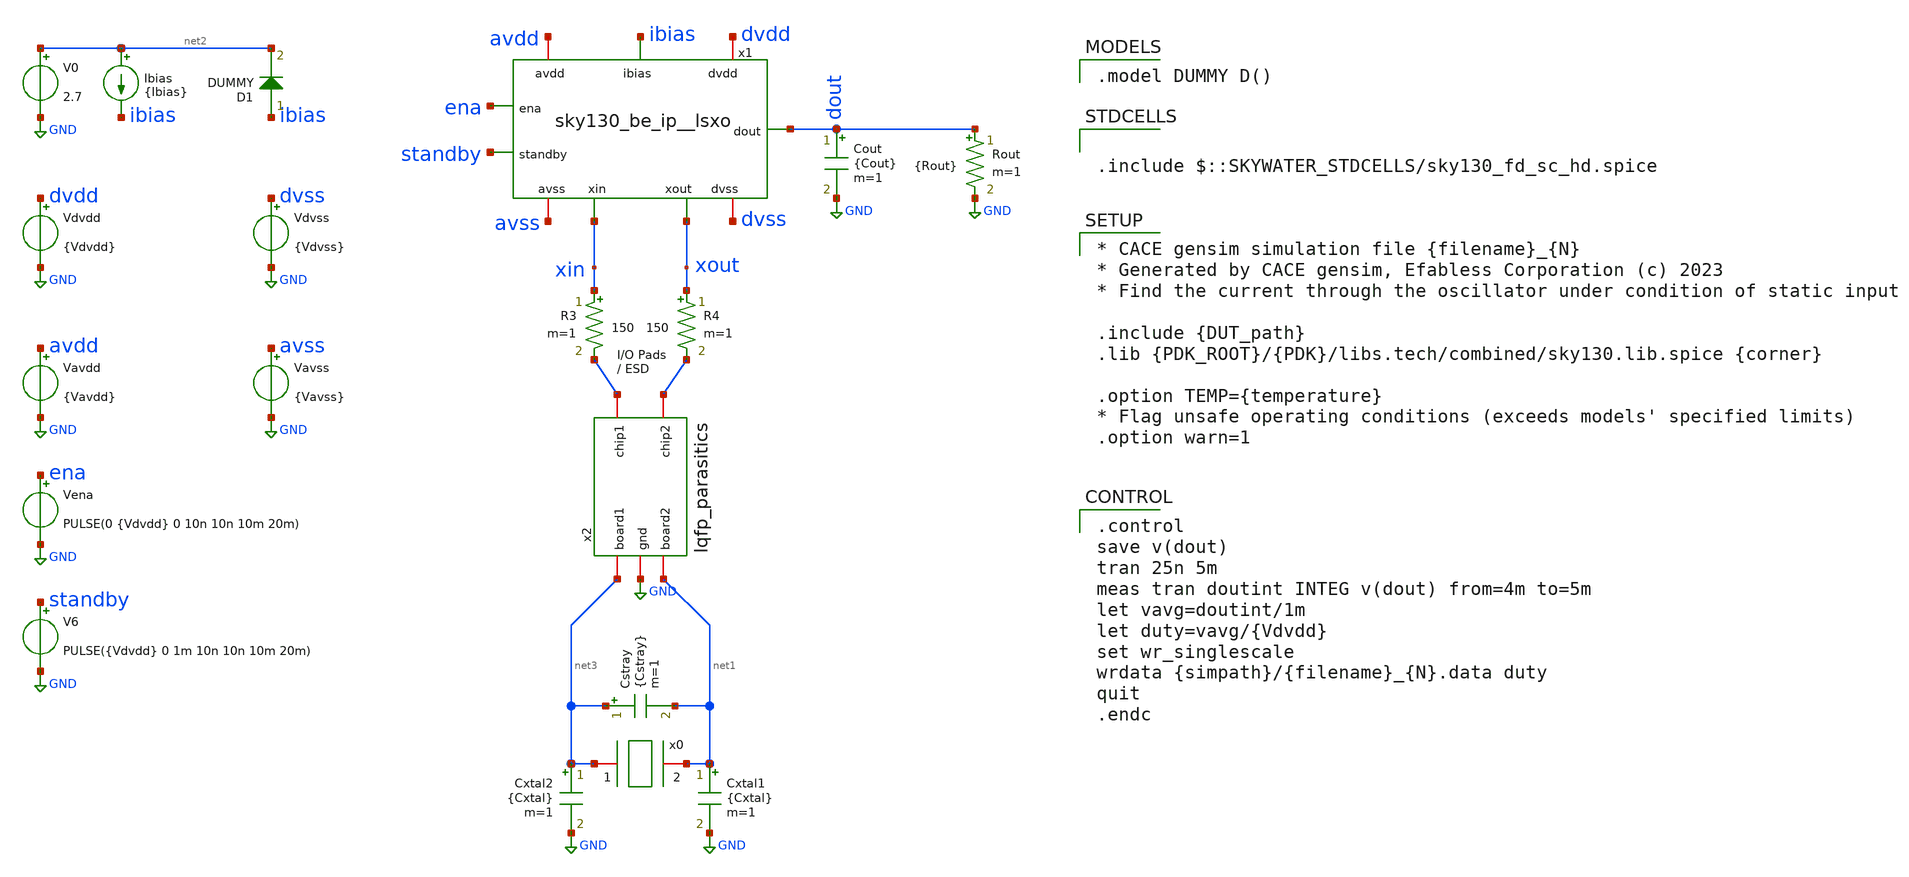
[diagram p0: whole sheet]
** sch_path: cace/tb_duty.sch

.include $::SKYWATER_STDCELLS/sky130_fd_sc_hd.spice

**.subckt tb_duty
Vdvdd dvdd GND {Vdvdd}
Vavdd avdd GND {Vavdd}
Cxtal2 net3 GND {Cxtal} m=1
Cxtal1 net1 GND {Cxtal} m=1
Cstray net3 net1 {Cstray} m=1
Ibias net2 ibias {Ibias}
Cout dout GND {Cout} m=1
V0 net2 GND 2.7
V6 standby GND PULSE({Vdvdd} 0 1m 10n 10n 10m 20m)
R3 xin net4 150 m=1
R4 xout net5 150 m=1
x2 net5 net4 GND net3 net1 lqfp_parasitics
Vena ena GND PULSE(0 {Vdvdd} 0 10n 10n 10m 20m)
D1 ibias net2 DUMMY area=100
x1 avdd avss dvdd dvss ibias ena standby dout xin xout sky130_be_ip__lsxo
Vdvss dvss GND {Vdvss}
Vavss avss GND {Vavss}
Rout dout GND {Rout} m=1
x0 net3 net1 xtal_iqd_125_1
**** begin user architecture code

.model DUMMY D()


.control
save v(dout)
tran 25n 5m
meas tran doutint INTEG v(dout) from=4m to=5m
let vavg=doutint/1m
let duty=vavg/{Vdvdd}
set wr_singlescale
wrdata {simpath}/{filename}_{N}.data duty
quit
.endc



* CACE gensim simulation file {filename}_{N}
* Generated by CACE gensim, Efabless Corporation (c) 2023
* Find the current through the oscillator under condition of static input

.include {DUT_path}
.lib {PDK_ROOT}/{PDK}/libs.tech/combined/sky130.lib.spice {corner}

.option TEMP={temperature}
* Flag unsafe operating conditions (exceeds models' specified limits)
.option warn=1


**** end user architecture code
**.ends
.GLOBAL GND
.end
